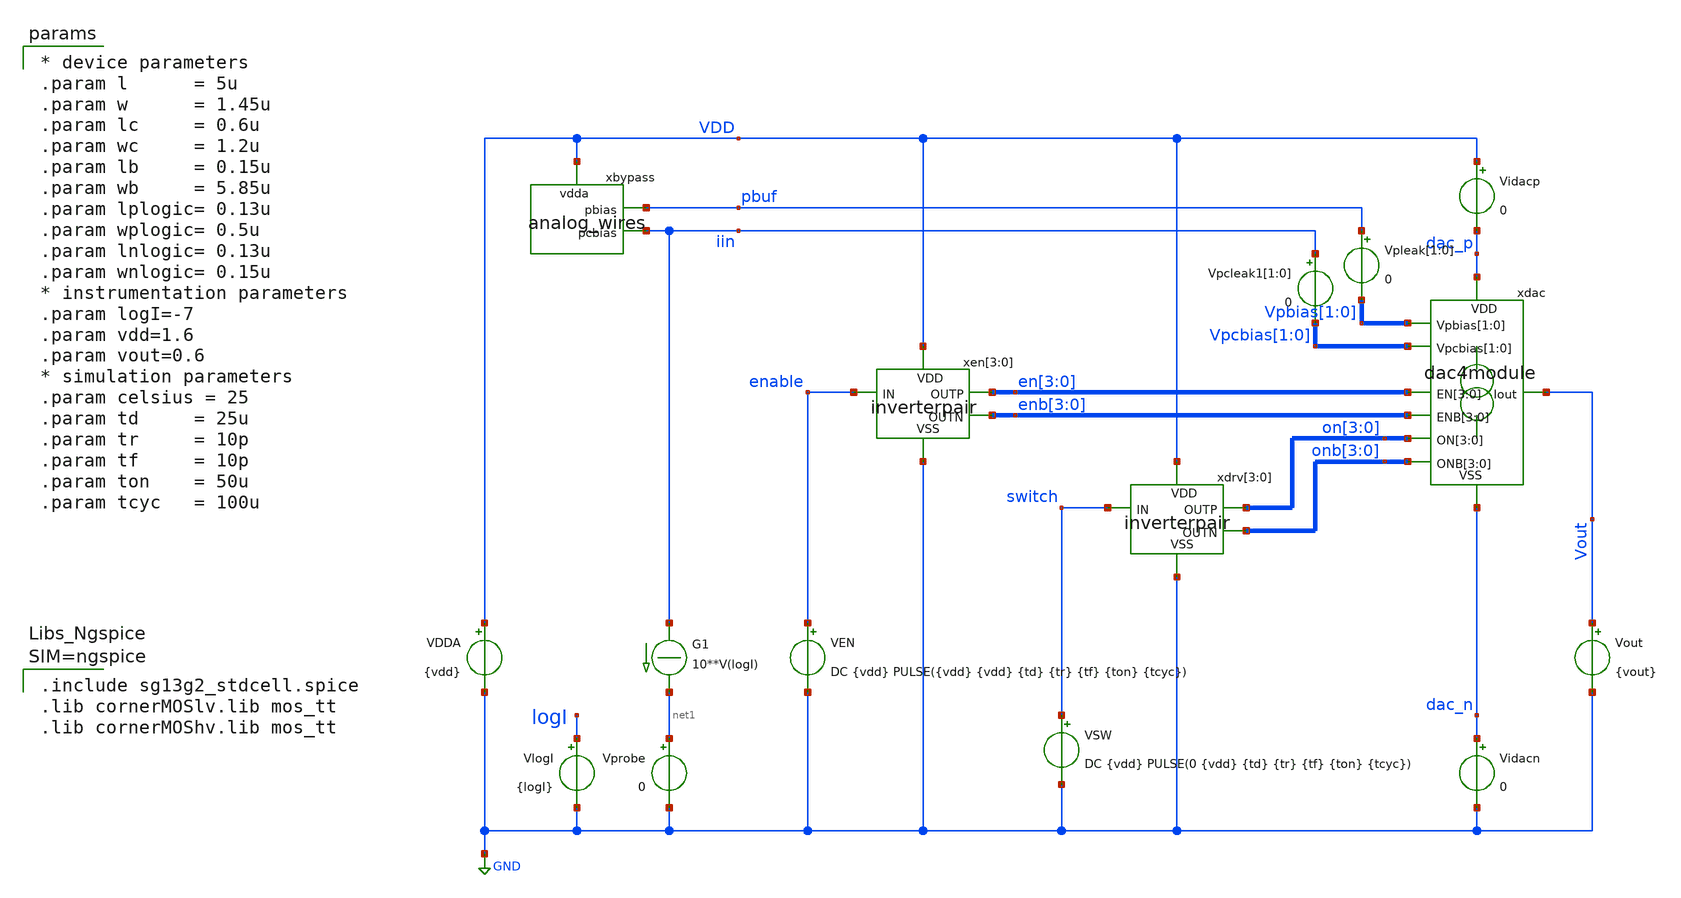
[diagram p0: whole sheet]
** sch_path: xschem/test_dac4_dc.sch
**.subckt test_dac4_dc
Vout Vout GND {vout}
.save i(vout)
Vprobe net1 GND 0
.save i(vprobe)
G1 iin net1 CUR=' 10**V(logI) '
VlogI logI GND {logI}
.save i(vlogi)
VDDA VDD GND {vdd}
.save i(vdda)
VSW switch GND DC {vdd} PULSE(0 {vdd} {td} {tr} {tf} {ton} {tcyc})
.save i(vsw)
Vidacp VDD dac_p 0
.save i(vidacp)
Vidacn dac_n GND 0
.save i(vidacn)
Vpleak[1] pbuf Vpbias[1] 0
Vpleak[0] pbuf Vpbias[0] 0
.save i(vpleak[1])
.save i(vpleak[0])
xdac dac_p en[3] en[2] en[1] en[0] enb[3] enb[2] enb[1] enb[0] on[3] on[2] on[1] on[0] onb[3] onb[2]
+ onb[1] onb[0] Vout Vpbias[1] Vpbias[0] Vpcbias[1] Vpcbias[0] dac_n dac4module
xbypass VDD pbuf iin analog_wires
Vpcleak1[1] iin Vpcbias[1] 0
Vpcleak1[0] iin Vpcbias[0] 0
.save i(vpcleak1[1])
.save i(vpcleak1[0])
xen[3] VDD en[3] enable enb[3] GND inverterpair
xen[2] VDD en[2] enable enb[2] GND inverterpair
xen[1] VDD en[1] enable enb[1] GND inverterpair
xen[0] VDD en[0] enable enb[0] GND inverterpair
xdrv[3] VDD on[3] switch onb[3] GND inverterpair
xdrv[2] VDD on[2] switch onb[2] GND inverterpair
xdrv[1] VDD on[1] switch onb[1] GND inverterpair
xdrv[0] VDD on[0] switch onb[0] GND inverterpair
VEN enable GND DC {vdd} PULSE({vdd} {vdd} {td} {tr} {tf} {ton} {tcyc})
.save i(ven)
**** begin user architecture code


.include test_dac4_dc.save
.temp=27
.options gmin=1e-15 abstol=1p method=gear
.options savecurrents
.control
save all
op
write test_dac4_dc.raw
set appendwrite
dc Vout 0 1.6 10m VlogI -8 -6 0.5
*tran 10n 500u
write test_dac4_dc.raw
plot title "output/reference current asymmetry"
+ 2*(vout#branch-vprobe#branch)/(vprobe#branch+vout#branch)
plot ylimit -6m 2m title "output/reference current asymmetry"
+ 2*(vout#branch-vprobe#branch)/(vprobe#branch+vout#branch)
plot vdd pbuf iin enable switch v("en[0]") v("enb[0]") v("on[0]") v("onb[0]") Vout
plot vout#branch vprobe#branch
*plot @n.xsw.xmbias.nsg13_lv_pmos[ids] @n.xsw.xmpullup.nsg13_lv_pmos[ids]
plot vidacp#branch vidacn#branch
*plot 0.5*(vidacp#branch+vidacn#branch) vidacp#branch-vidacn#branch
.endc




.include sg13g2_stdcell.spice
.lib cornerMOSlv.lib mos_tt
.lib cornerMOShv.lib mos_tt



* device parameters
.param l      = 5u
.param w      = 1.45u
.param lc     = 0.6u
.param wc     = 1.2u
.param lb     = 0.15u
.param wb     = 5.85u
.param lplogic= 0.13u
.param wplogic= 0.5u
.param lnlogic= 0.13u
.param wnlogic= 0.15u
* instrumentation parameters
.param logI=-7
.param vdd=1.6
.param vout=0.6
* simulation parameters
.param celsius = 25
.param td     = 25u
.param tr     = 10p
.param tf     = 10p
.param ton    = 50u
.param tcyc   = 100u


**** end user architecture code
**.ends

* expanding   symbol:  dac4module.sym # of pins=9
** sym_path: xschem/dac4module.sym
** sch_path: xschem/dac4module.sch
.subckt dac4module VDD EN[3] EN[2] EN[1] EN[0] ENB[3] ENB[2] ENB[1] ENB[0] ON[3] ON[2] ON[1] ON[0]
+ ONB[3] ONB[2] ONB[1] ONB[0] Iout Vpbias[1] Vpbias[0] Vpcbias[1] Vpcbias[0] VSS
*.opin Iout
*.ipin ON[3],ON[2],ON[1],ON[0]
*.ipin ONB[3],ONB[2],ONB[1],ONB[0]
*.iopin VSS
*.iopin VDD
*.iopin Vpcbias[1],Vpcbias[0]
*.ipin EN[3],EN[2],EN[1],EN[0]
*.ipin ENB[3],ENB[2],ENB[1],ENB[0]
*.iopin Vpbias[1],Vpbias[0]
XMcbias[0] Vpcbias[0] Vpcbias[0] Vpbias[0] VDD sg13_lv_pmos w=5.85u l=0.15u ng=1 m=2 mm_ok=1
**** begin user architecture code

* device parameters
.param l      = 5u
.param w      = 1.45u
.param lc     = 0.6u
.param wc     = 1.2u
.param lb     = 0.15u
.param wb     = 5.85u
.param lplogic= 0.13u
.param wplogic= 0.5u
.param lnlogic= 0.13u
.param wnlogic= 0.15u


**** end user architecture code
xref[1] VDD Vpbias[0] EN[1] ENB[1] Vpbias[0] Vpcbias[0] VSS unitsource2u
xref[0] VDD Vpbias[0] EN[0] ENB[0] Vpbias[0] Vpcbias[0] VSS unitsource2u
xsrc[1] VDD Vpbias[0] ON[1] ONB[1] Iout Vpcbias[0] VSS unitsource2u
xsrc[0] VDD Vpbias[0] ON[0] ONB[0] Iout Vpcbias[0] VSS unitsource2u
XMcbias[1] Vpcbias[1] Vpcbias[1] Vpbias[1] VDD sg13_lv_pmos w=5.85u l=0.15u ng=1 m=2 mm_ok=1
xref1[3] VDD Vpbias[1] EN[3] ENB[3] Vpbias[1] Vpcbias[1] VSS unitsource2u
xref1[2] VDD Vpbias[1] EN[2] ENB[2] Vpbias[1] Vpcbias[1] VSS unitsource2u
xsrc1[3] VDD Vpbias[1] ON[3] ONB[3] Iout Vpcbias[1] VSS unitsource2u
xsrc1[2] VDD Vpbias[1] ON[2] ONB[2] Iout Vpcbias[1] VSS unitsource2u
* tap: EN[3:0] --> EN[1:0]
* tap: ENB[3:0] --> ENB[1:0]
* tap: ENB[3:0] --> ENB[3:2]
* tap: EN[3:0] --> EN[3:2]
* tap: ON[3:0] --> ON[1:0]
* tap: ONB[3:0] --> ONB[1:0]
* tap: ON[3:0] --> ON[3:2]
* tap: ONB[3:0] --> ONB[3:2]
* tap: Vpbias[1:0] --> Vpbias[0]
* tap: Vpcbias[1:0] --> Vpcbias[0]
* tap: Vpbias[1:0] --> Vpbias[1]
* tap: Vpcbias[1:0] --> Vpcbias[1]
.ends


* expanding   symbol:  analog_wires.sym # of pins=3
** sym_path: xschem/analog_wires.sym
** sch_path: xschem/analog_wires.sch
.subckt analog_wires vdda pbias pcbias
*.iopin vdda
*.iopin pcbias
*.iopin pbias
XMcbuffer vdda pcbias vdda vdda sg13_hv_pmos w=8u l=8u ng=1 m=19 mm_ok=1
XMbbuffer vdda pbias vdda vdda sg13_hv_pmos w=8u l=8u ng=1 m=19 mm_ok=1
.ends


* expanding   symbol:  inverterpair.sym # of pins=5
** sym_path: xschem/inverterpair.sym
** sch_path: xschem/inverterpair.sch
.subckt inverterpair VDD OUTP IN OUTN VSS
*.iopin VSS
*.ipin IN
*.opin OUTN
*.opin OUTP
*.iopin VDD
xinv2 OUTP OUTN VDD VSS sg13g2_inv_1
xinv1 OUTN IN VDD VSS sg13g2_inv_1
.ends


* expanding   symbol:  unitsource2u.sym # of pins=7
** sym_path: xschem/unitsource2u.sym
** sch_path: xschem/unitsource2u.sch
.subckt unitsource2u VDD VbiasP ON ONB Iout VcascP VSS
*.iopin VSS
*.iopin VDD
*.iopin VbiasP
*.iopin VcascP
*.ipin ON
*.ipin ONB
*.iopin Iout
xnonoverlap VDD VSS ON ONB on_n off_n nonoverlap
xsw VDD off_n Vcasc on_n VcascP cascodeswitch_pmos
xsrc VDD VbiasP Vcasc Iout pcsource2u
.ends


* expanding   symbol:  sg13g2_stdcells/sg13g2_inv_1.sym # of pins=2
** sym_path: sg13g2_stdcells/sg13g2_inv_1.sym
** sch_path: sg13g2_stdcells/sg13g2_inv_1.sch
.subckt sg13g2_inv_1 Y A VDD VSS
*.opin Y
*.ipin A
*.iopin VDD
*.iopin VSS
XM1 Y A VSS VSS sg13_lv_nmos w=740.00n l=130.00n ng=1 m=1 mm_ok=1
XM2 Y A VDD VDD sg13_lv_pmos w=1.12u l=130.00n ng=1 m=1 mm_ok=1
.ends


* expanding   symbol:  nonoverlap.sym # of pins=6
** sym_path: xschem/nonoverlap.sym
** sch_path: xschem/nonoverlap.sch
.subckt nonoverlap VDD VSS INP INN OUTN OUTP
*.iopin VSS
*.iopin VDD
*.ipin INP
*.ipin INN
*.opin OUTP
*.opin OUTN
XM1 OUTN INP VDD VDD sg13_lv_pmos w=0.3u l=0.13u ng=1 m=1 mm_ok=1
XM2 OUTP INN VDD VDD sg13_lv_pmos w=0.3u l=0.13u ng=1 m=1 mm_ok=1
XM3 OUTN OUTP VSS VSS sg13_lv_nmos w=0.15u l=0.52u ng=1 m=1 mm_ok=1
XM4 OUTP OUTN VSS VSS sg13_lv_nmos w=0.15u l=0.52u ng=1 m=1 mm_ok=1
.ends


* expanding   symbol:  cascodeswitch_pmos.sym # of pins=5
** sym_path: xschem/cascodeswitch_pmos.sym
** sch_path: xschem/cascodeswitch_pmos.sch
.subckt cascodeswitch_pmos VDD off_n Vcasc on_n Vbpcasc
*.ipin off_n
*.ipin Vbpcasc
*.opin Vcasc
*.ipin on_n
*.ipin VDD
XMpullup Vcasc off_n VDD VDD sg13_lv_pmos w=0.3u l=0.13u ng=1 m=1 mm_ok=1
XMbias Vbpcasc on_n Vcasc VDD sg13_lv_pmos w=0.3u l=0.13u ng=1 m=1 mm_ok=1
.ends


* expanding   symbol:  pcsource2u.sym # of pins=4
** sym_path: xschem/pcsource2u.sym
** sch_path: xschem/pcsource2u.sch
.subckt pcsource2u VDD VbiasP VcascodeP Iout
*.ipin VcascodeP
*.ipin VbiasP
*.opin Iout
*.ipin VDD
XMsrc drain net4 VDD net1 sg13_lv_pmos w=1.45u l=5u ng=1 m=1 mm_ok=1
XMcasc Iout net3 drain net2 sg13_lv_pmos w=1.2u l=0.6u ng=1 m=1 mm_ok=1
Vgsrc net4 VbiasP 0
.save i(vgsrc)
Vgcasc net3 VcascodeP 0
.save i(vgcasc)
Vbsrc VDD net1 0
.save i(vbsrc)
Vbcasc VDD net2 0
.save i(vbcasc)
.ends

.GLOBAL GND
.end
